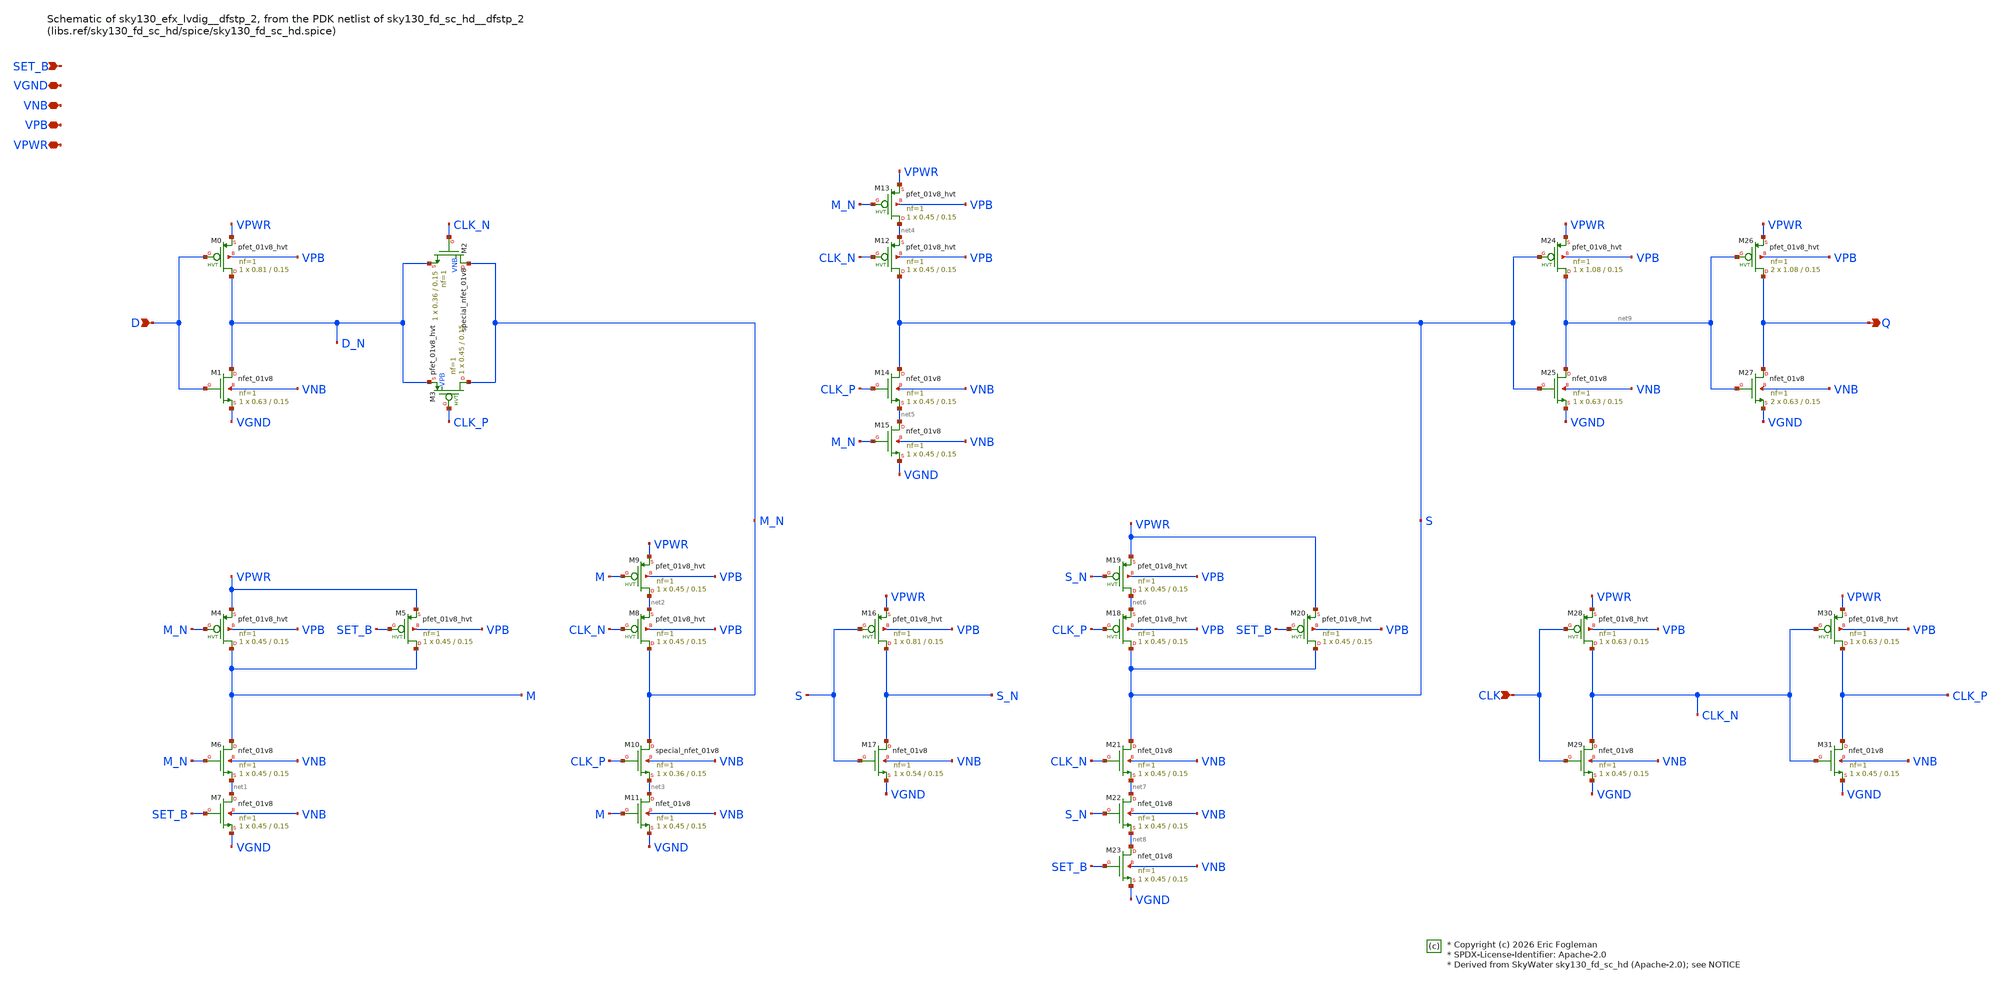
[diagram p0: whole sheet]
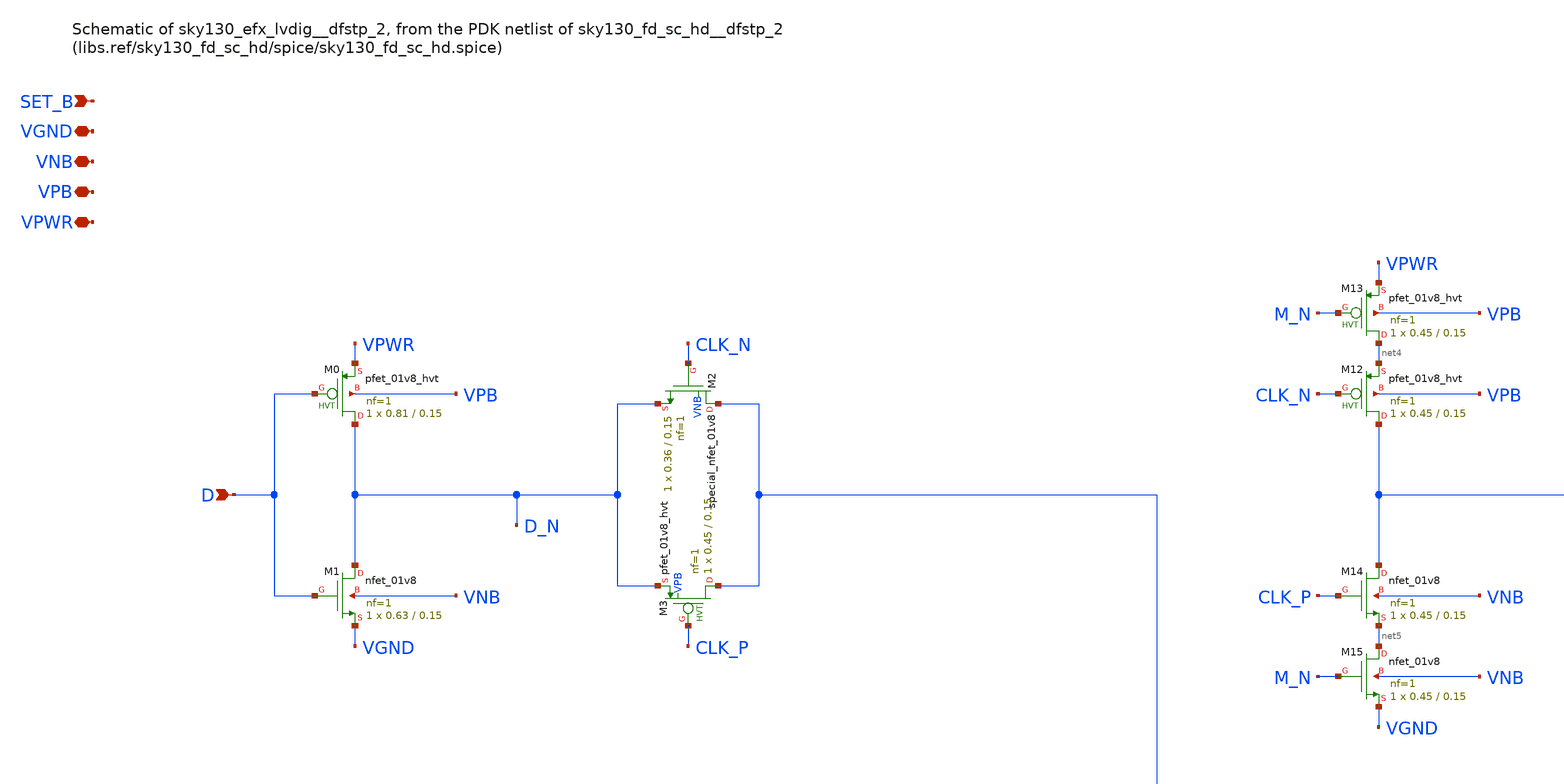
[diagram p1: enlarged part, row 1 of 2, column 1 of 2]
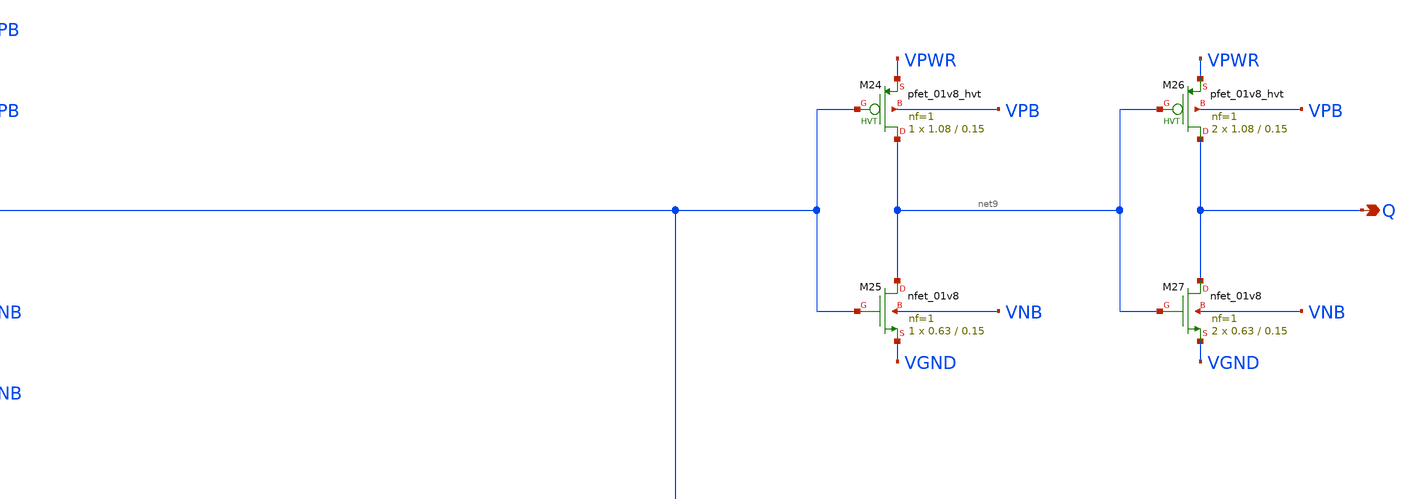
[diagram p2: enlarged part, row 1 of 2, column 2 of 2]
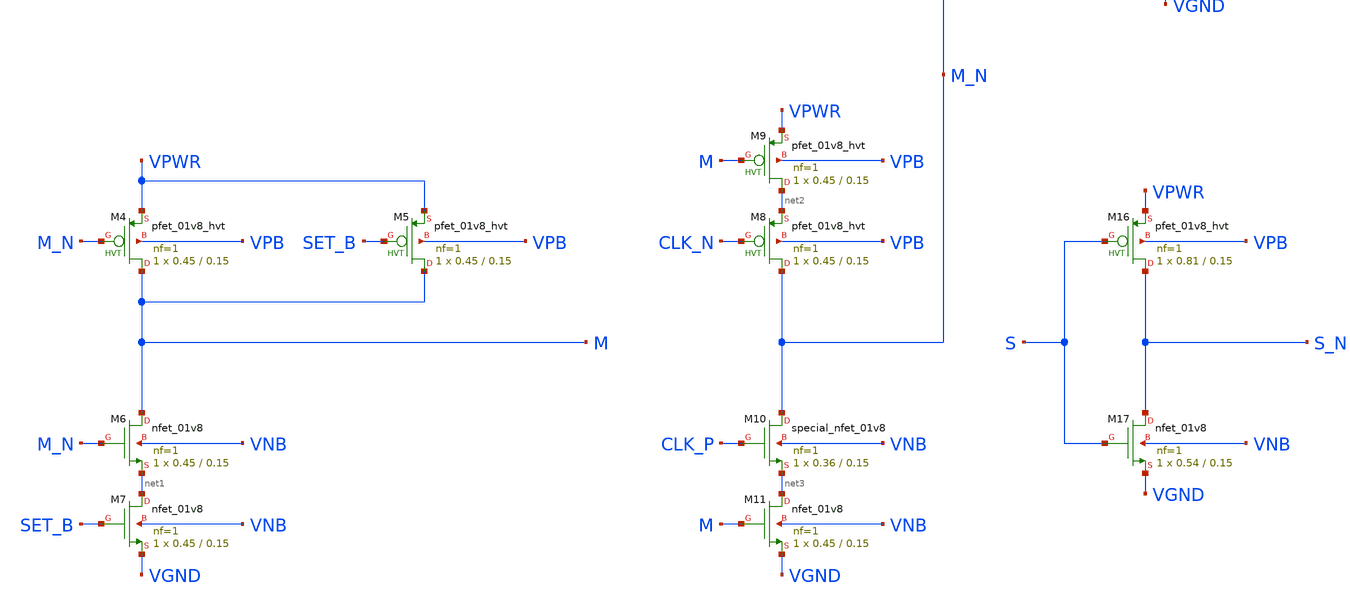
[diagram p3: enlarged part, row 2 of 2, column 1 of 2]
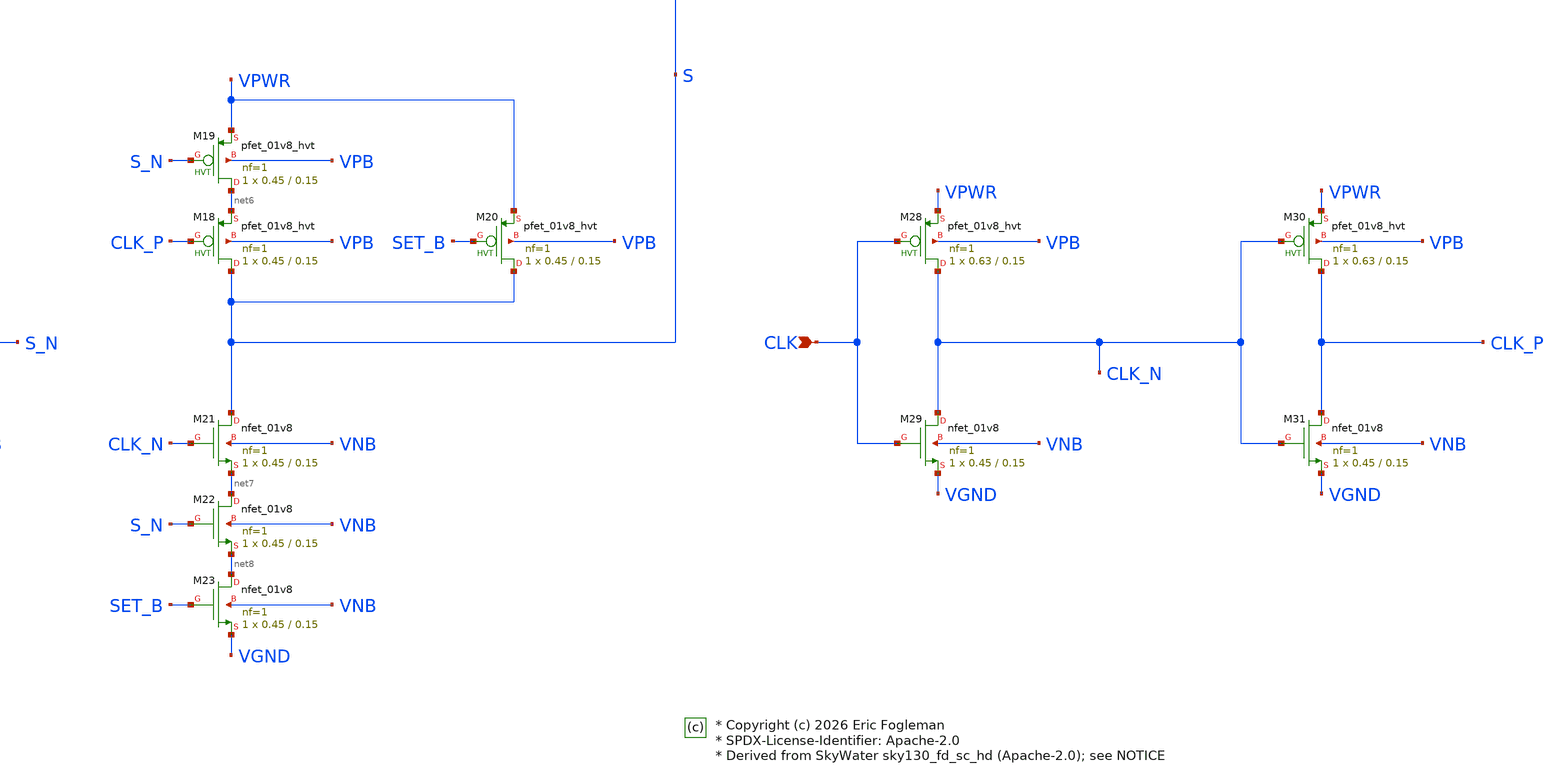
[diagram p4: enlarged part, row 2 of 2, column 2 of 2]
** sch_path: xschem/sky130_efx_lvdig__dfstp_2.sch

* Copyright (c) 2026 Eric Fogleman
* SPDX-License-Identifier: Apache-2.0
* Derived from SkyWater sky130_fd_sc_hd (Apache-2.0); see NOTICE

**.subckt sky130_efx_lvdig__dfstp_2 D Q CLK SET_B VGND VNB VPB VPWR
*.ipin D
*.opin Q
*.ipin CLK
*.ipin SET_B
*.iopin VGND
*.iopin VNB
*.iopin VPB
*.iopin VPWR
XM0 D_N D VPWR VPB sky130_fd_pr__pfet_01v8_hvt L=0.15 W=0.81 nf=1 ad='int((1 + 1)/2) * 0.81 / 1 * 0.29'
+ as='int((1 + 2)/2) * 0.81 / 1 * 0.29' pd='2*int((1 + 1)/2) * (0.81 / 1 + 0.29)' ps='2*int((1 + 2)/2) * (0.81 / 1 + 0.29)'
+ nrd='0.29 / 0.81 ' nrs='0.29 / 0.81 ' sa=0 sb=0 sd=0 mult=1 m=1
XM1 D_N D VGND VNB sky130_fd_pr__nfet_01v8 L=0.15 W=0.63 nf=1 ad='int((1 + 1)/2) * 0.63 / 1 * 0.29' as='int((1 + 2)/2) * 0.63 / 1 * 0.29'
+ pd='2*int((1 + 1)/2) * (0.63 / 1 + 0.29)' ps='2*int((1 + 2)/2) * (0.63 / 1 + 0.29)' nrd='0.29 / 0.63 '
+ nrs='0.29 / 0.63 ' sa=0 sb=0 sd=0 mult=1 m=1
XM2 M_N CLK_N D_N VNB sky130_fd_pr__special_nfet_01v8 L=0.15 W=0.36 nf=1 ad='int((nf+1)/2) * W/nf * 0.29'
+ as='int((nf+2)/2) * W/nf * 0.29' pd='2*int((nf+1)/2) * (W/nf + 0.29)' ps='2*int((nf+2)/2) * (W/nf + 0.29)'
+ nrd='0.29 / W' nrs='0.29 / W' sa=0 sb=0 sd=0 mult=1 m=1
XM3 M_N CLK_P D_N VPB sky130_fd_pr__pfet_01v8_hvt L=0.15 W=0.45 nf=1 ad='int((1 + 1)/2) * 0.45 / 1 * 0.29'
+ as='int((1 + 2)/2) * 0.45 / 1 * 0.29' pd='2*int((1 + 1)/2) * (0.45 / 1 + 0.29)' ps='2*int((1 + 2)/2) * (0.45 / 1 + 0.29)'
+ nrd='0.29 / 0.45 ' nrs='0.29 / 0.45 ' sa=0 sb=0 sd=0 mult=1 m=1
XM4 M M_N VPWR VPB sky130_fd_pr__pfet_01v8_hvt L=0.15 W=0.45 nf=1 ad='int((1 + 1)/2) * 0.45 / 1 * 0.29'
+ as='int((1 + 2)/2) * 0.45 / 1 * 0.29' pd='2*int((1 + 1)/2) * (0.45 / 1 + 0.29)' ps='2*int((1 + 2)/2) * (0.45 / 1 + 0.29)'
+ nrd='0.29 / 0.45 ' nrs='0.29 / 0.45 ' sa=0 sb=0 sd=0 mult=1 m=1
XM5 M SET_B VPWR VPB sky130_fd_pr__pfet_01v8_hvt L=0.15 W=0.45 nf=1 ad='int((1 + 1)/2) * 0.45 / 1 * 0.29'
+ as='int((1 + 2)/2) * 0.45 / 1 * 0.29' pd='2*int((1 + 1)/2) * (0.45 / 1 + 0.29)' ps='2*int((1 + 2)/2) * (0.45 / 1 + 0.29)'
+ nrd='0.29 / 0.45 ' nrs='0.29 / 0.45 ' sa=0 sb=0 sd=0 mult=1 m=1
XM6 M M_N net1 VNB sky130_fd_pr__nfet_01v8 L=0.15 W=0.45 nf=1 ad='int((1 + 1)/2) * 0.45 / 1 * 0.29' as='int((1 + 2)/2) * 0.45 / 1 * 0.29'
+ pd='2*int((1 + 1)/2) * (0.45 / 1 + 0.29)' ps='2*int((1 + 2)/2) * (0.45 / 1 + 0.29)' nrd='0.29 / 0.45 '
+ nrs='0.29 / 0.45 ' sa=0 sb=0 sd=0 mult=1 m=1
XM7 net1 SET_B VGND VNB sky130_fd_pr__nfet_01v8 L=0.15 W=0.45 nf=1 ad='int((1 + 1)/2) * 0.45 / 1 * 0.29'
+ as='int((1 + 2)/2) * 0.45 / 1 * 0.29' pd='2*int((1 + 1)/2) * (0.45 / 1 + 0.29)' ps='2*int((1 + 2)/2) * (0.45 / 1 + 0.29)'
+ nrd='0.29 / 0.45 ' nrs='0.29 / 0.45 ' sa=0 sb=0 sd=0 mult=1 m=1
XM8 M_N CLK_N net2 VPB sky130_fd_pr__pfet_01v8_hvt L=0.15 W=0.45 nf=1 ad='int((1 + 1)/2) * 0.45 / 1 * 0.29'
+ as='int((1 + 2)/2) * 0.45 / 1 * 0.29' pd='2*int((1 + 1)/2) * (0.45 / 1 + 0.29)' ps='2*int((1 + 2)/2) * (0.45 / 1 + 0.29)'
+ nrd='0.29 / 0.45 ' nrs='0.29 / 0.45 ' sa=0 sb=0 sd=0 mult=1 m=1
XM9 net2 M VPWR VPB sky130_fd_pr__pfet_01v8_hvt L=0.15 W=0.45 nf=1 ad='int((1 + 1)/2) * 0.45 / 1 * 0.29'
+ as='int((1 + 2)/2) * 0.45 / 1 * 0.29' pd='2*int((1 + 1)/2) * (0.45 / 1 + 0.29)' ps='2*int((1 + 2)/2) * (0.45 / 1 + 0.29)'
+ nrd='0.29 / 0.45 ' nrs='0.29 / 0.45 ' sa=0 sb=0 sd=0 mult=1 m=1
XM10 M_N CLK_P net3 VNB sky130_fd_pr__special_nfet_01v8 L=0.15 W=0.36 nf=1 ad='int((1 + 1)/2) * 0.36 / 1 * 0.29'
+ as='int((1 + 2)/2) * 0.36 / 1 * 0.29' pd='2*int((1 + 1)/2) * (0.36 / 1 + 0.29)' ps='2*int((1 + 2)/2) * (0.36 / 1 + 0.29)'
+ nrd='0.29 / 0.36 ' nrs='0.29 / 0.36 ' sa=0 sb=0 sd=0 mult=1 m=1
XM11 net3 M VGND VNB sky130_fd_pr__nfet_01v8 L=0.15 W=0.45 nf=1 ad='int((1 + 1)/2) * 0.45 / 1 * 0.29'
+ as='int((1 + 2)/2) * 0.45 / 1 * 0.29' pd='2*int((1 + 1)/2) * (0.45 / 1 + 0.29)' ps='2*int((1 + 2)/2) * (0.45 / 1 + 0.29)'
+ nrd='0.29 / 0.45 ' nrs='0.29 / 0.45 ' sa=0 sb=0 sd=0 mult=1 m=1
XM12 S CLK_N net4 VPB sky130_fd_pr__pfet_01v8_hvt L=0.15 W=0.45 nf=1 ad='int((1 + 1)/2) * 0.45 / 1 * 0.29'
+ as='int((1 + 2)/2) * 0.45 / 1 * 0.29' pd='2*int((1 + 1)/2) * (0.45 / 1 + 0.29)' ps='2*int((1 + 2)/2) * (0.45 / 1 + 0.29)'
+ nrd='0.29 / 0.45 ' nrs='0.29 / 0.45 ' sa=0 sb=0 sd=0 mult=1 m=1
XM13 net4 M_N VPWR VPB sky130_fd_pr__pfet_01v8_hvt L=0.15 W=0.45 nf=1 ad='int((1 + 1)/2) * 0.45 / 1 * 0.29'
+ as='int((1 + 2)/2) * 0.45 / 1 * 0.29' pd='2*int((1 + 1)/2) * (0.45 / 1 + 0.29)' ps='2*int((1 + 2)/2) * (0.45 / 1 + 0.29)'
+ nrd='0.29 / 0.45 ' nrs='0.29 / 0.45 ' sa=0 sb=0 sd=0 mult=1 m=1
XM14 S CLK_P net5 VNB sky130_fd_pr__nfet_01v8 L=0.15 W=0.45 nf=1 ad='int((1 + 1)/2) * 0.45 / 1 * 0.29'
+ as='int((1 + 2)/2) * 0.45 / 1 * 0.29' pd='2*int((1 + 1)/2) * (0.45 / 1 + 0.29)' ps='2*int((1 + 2)/2) * (0.45 / 1 + 0.29)'
+ nrd='0.29 / 0.45 ' nrs='0.29 / 0.45 ' sa=0 sb=0 sd=0 mult=1 m=1
XM15 net5 M_N VGND VNB sky130_fd_pr__nfet_01v8 L=0.15 W=0.45 nf=1 ad='int((1 + 1)/2) * 0.45 / 1 * 0.29'
+ as='int((1 + 2)/2) * 0.45 / 1 * 0.29' pd='2*int((1 + 1)/2) * (0.45 / 1 + 0.29)' ps='2*int((1 + 2)/2) * (0.45 / 1 + 0.29)'
+ nrd='0.29 / 0.45 ' nrs='0.29 / 0.45 ' sa=0 sb=0 sd=0 mult=1 m=1
XM16 S_N S VPWR VPB sky130_fd_pr__pfet_01v8_hvt L=0.15 W=0.81 nf=1 ad='int((1 + 1)/2) * 0.81 / 1 * 0.29'
+ as='int((1 + 2)/2) * 0.81 / 1 * 0.29' pd='2*int((1 + 1)/2) * (0.81 / 1 + 0.29)' ps='2*int((1 + 2)/2) * (0.81 / 1 + 0.29)'
+ nrd='0.29 / 0.81 ' nrs='0.29 / 0.81 ' sa=0 sb=0 sd=0 mult=1 m=1
XM17 S_N S VGND VNB sky130_fd_pr__nfet_01v8 L=0.15 W=0.54 nf=1 ad='int((1 + 1)/2) * 0.54 / 1 * 0.29'
+ as='int((1 + 2)/2) * 0.54 / 1 * 0.29' pd='2*int((1 + 1)/2) * (0.54 / 1 + 0.29)' ps='2*int((1 + 2)/2) * (0.54 / 1 + 0.29)'
+ nrd='0.29 / 0.54 ' nrs='0.29 / 0.54 ' sa=0 sb=0 sd=0 mult=1 m=1
XM18 S CLK_P net6 VPB sky130_fd_pr__pfet_01v8_hvt L=0.15 W=0.45 nf=1 ad='int((1 + 1)/2) * 0.45 / 1 * 0.29'
+ as='int((1 + 2)/2) * 0.45 / 1 * 0.29' pd='2*int((1 + 1)/2) * (0.45 / 1 + 0.29)' ps='2*int((1 + 2)/2) * (0.45 / 1 + 0.29)'
+ nrd='0.29 / 0.45 ' nrs='0.29 / 0.45 ' sa=0 sb=0 sd=0 mult=1 m=1
XM19 net6 S_N VPWR VPB sky130_fd_pr__pfet_01v8_hvt L=0.15 W=0.45 nf=1 ad='int((1 + 1)/2) * 0.45 / 1 * 0.29'
+ as='int((1 + 2)/2) * 0.45 / 1 * 0.29' pd='2*int((1 + 1)/2) * (0.45 / 1 + 0.29)' ps='2*int((1 + 2)/2) * (0.45 / 1 + 0.29)'
+ nrd='0.29 / 0.45 ' nrs='0.29 / 0.45 ' sa=0 sb=0 sd=0 mult=1 m=1
XM20 S SET_B VPWR VPB sky130_fd_pr__pfet_01v8_hvt L=0.15 W=0.45 nf=1 ad='int((1 + 1)/2) * 0.45 / 1 * 0.29'
+ as='int((1 + 2)/2) * 0.45 / 1 * 0.29' pd='2*int((1 + 1)/2) * (0.45 / 1 + 0.29)' ps='2*int((1 + 2)/2) * (0.45 / 1 + 0.29)'
+ nrd='0.29 / 0.45 ' nrs='0.29 / 0.45 ' sa=0 sb=0 sd=0 mult=1 m=1
XM21 S CLK_N net7 VNB sky130_fd_pr__nfet_01v8 L=0.15 W=0.45 nf=1 ad='int((1 + 1)/2) * 0.45 / 1 * 0.29'
+ as='int((1 + 2)/2) * 0.45 / 1 * 0.29' pd='2*int((1 + 1)/2) * (0.45 / 1 + 0.29)' ps='2*int((1 + 2)/2) * (0.45 / 1 + 0.29)'
+ nrd='0.29 / 0.45 ' nrs='0.29 / 0.45 ' sa=0 sb=0 sd=0 mult=1 m=1
XM22 net7 S_N net8 VNB sky130_fd_pr__nfet_01v8 L=0.15 W=0.45 nf=1 ad='int((1 + 1)/2) * 0.45 / 1 * 0.29'
+ as='int((1 + 2)/2) * 0.45 / 1 * 0.29' pd='2*int((1 + 1)/2) * (0.45 / 1 + 0.29)' ps='2*int((1 + 2)/2) * (0.45 / 1 + 0.29)'
+ nrd='0.29 / 0.45 ' nrs='0.29 / 0.45 ' sa=0 sb=0 sd=0 mult=1 m=1
XM23 net8 SET_B VGND VNB sky130_fd_pr__nfet_01v8 L=0.15 W=0.45 nf=1 ad='int((1 + 1)/2) * 0.45 / 1 * 0.29'
+ as='int((1 + 2)/2) * 0.45 / 1 * 0.29' pd='2*int((1 + 1)/2) * (0.45 / 1 + 0.29)' ps='2*int((1 + 2)/2) * (0.45 / 1 + 0.29)'
+ nrd='0.29 / 0.45 ' nrs='0.29 / 0.45 ' sa=0 sb=0 sd=0 mult=1 m=1
XM24 net9 S VPWR VPB sky130_fd_pr__pfet_01v8_hvt L=0.15 W=1.08 nf=1 ad='int((1 + 1)/2) * 1.08 / 1 * 0.29'
+ as='int((1 + 2)/2) * 1.08 / 1 * 0.29' pd='2*int((1 + 1)/2) * (1.08 / 1 + 0.29)' ps='2*int((1 + 2)/2) * (1.08 / 1 + 0.29)'
+ nrd='0.29 / 1.08 ' nrs='0.29 / 1.08 ' sa=0 sb=0 sd=0 mult=1 m=1
XM25 net9 S VGND VNB sky130_fd_pr__nfet_01v8 L=0.15 W=0.63 nf=1 ad='int((1 + 1)/2) * 0.63 / 1 * 0.29'
+ as='int((1 + 2)/2) * 0.63 / 1 * 0.29' pd='2*int((1 + 1)/2) * (0.63 / 1 + 0.29)' ps='2*int((1 + 2)/2) * (0.63 / 1 + 0.29)'
+ nrd='0.29 / 0.63 ' nrs='0.29 / 0.63 ' sa=0 sb=0 sd=0 mult=1 m=1
XM26 Q net9 VPWR VPB sky130_fd_pr__pfet_01v8_hvt L=0.15 W=1.08 nf=1 ad='int((1 + 1)/2) * 1.08 / 1 * 0.29'
+ as='int((1 + 2)/2) * 1.08 / 1 * 0.29' pd='2*int((1 + 1)/2) * (1.08 / 1 + 0.29)' ps='2*int((1 + 2)/2) * (1.08 / 1 + 0.29)'
+ nrd='0.29 / 1.08 ' nrs='0.29 / 1.08 ' sa=0 sb=0 sd=0 mult=2 m=2
XM27 Q net9 VGND VNB sky130_fd_pr__nfet_01v8 L=0.15 W=0.63 nf=1 ad='int((1 + 1)/2) * 0.63 / 1 * 0.29'
+ as='int((1 + 2)/2) * 0.63 / 1 * 0.29' pd='2*int((1 + 1)/2) * (0.63 / 1 + 0.29)' ps='2*int((1 + 2)/2) * (0.63 / 1 + 0.29)'
+ nrd='0.29 / 0.63 ' nrs='0.29 / 0.63 ' sa=0 sb=0 sd=0 mult=2 m=2
XM28 CLK_N CLK VPWR VPB sky130_fd_pr__pfet_01v8_hvt L=0.15 W=0.63 nf=1 ad='int((1 + 1)/2) * 0.63 / 1 * 0.29'
+ as='int((1 + 2)/2) * 0.63 / 1 * 0.29' pd='2*int((1 + 1)/2) * (0.63 / 1 + 0.29)' ps='2*int((1 + 2)/2) * (0.63 / 1 + 0.29)'
+ nrd='0.29 / 0.63 ' nrs='0.29 / 0.63 ' sa=0 sb=0 sd=0 mult=1 m=1
XM29 CLK_N CLK VGND VNB sky130_fd_pr__nfet_01v8 L=0.15 W=0.45 nf=1 ad='int((1 + 1)/2) * 0.45 / 1 * 0.29'
+ as='int((1 + 2)/2) * 0.45 / 1 * 0.29' pd='2*int((1 + 1)/2) * (0.45 / 1 + 0.29)' ps='2*int((1 + 2)/2) * (0.45 / 1 + 0.29)'
+ nrd='0.29 / 0.45 ' nrs='0.29 / 0.45 ' sa=0 sb=0 sd=0 mult=1 m=1
XM30 CLK_P CLK_N VPWR VPB sky130_fd_pr__pfet_01v8_hvt L=0.15 W=0.63 nf=1 ad='int((1 + 1)/2) * 0.63 / 1 * 0.29'
+ as='int((1 + 2)/2) * 0.63 / 1 * 0.29' pd='2*int((1 + 1)/2) * (0.63 / 1 + 0.29)' ps='2*int((1 + 2)/2) * (0.63 / 1 + 0.29)'
+ nrd='0.29 / 0.63 ' nrs='0.29 / 0.63 ' sa=0 sb=0 sd=0 mult=1 m=1
XM31 CLK_P CLK_N VGND VNB sky130_fd_pr__nfet_01v8 L=0.15 W=0.45 nf=1 ad='int((1 + 1)/2) * 0.45 / 1 * 0.29'
+ as='int((1 + 2)/2) * 0.45 / 1 * 0.29' pd='2*int((1 + 1)/2) * (0.45 / 1 + 0.29)' ps='2*int((1 + 2)/2) * (0.45 / 1 + 0.29)'
+ nrd='0.29 / 0.45 ' nrs='0.29 / 0.45 ' sa=0 sb=0 sd=0 mult=1 m=1
**.ends
.end
